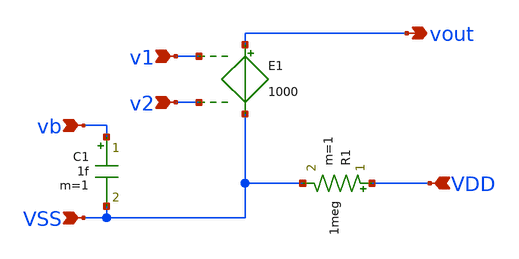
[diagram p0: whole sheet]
** sch_path: xschem/ideal_diffamp_nmos.sch
**.subckt ideal_diffamp_nmos v1 v2 VSS VDD vb vout
*.ipin v1
*.ipin v2
*.ipin VSS
*.ipin VDD
*.ipin vb
*.opin vout
E1 vout VSS v1 v2 1000
R1 VDD VSS 1meg m=1
C1 vb VSS 1f m=1
**.ends
.end
